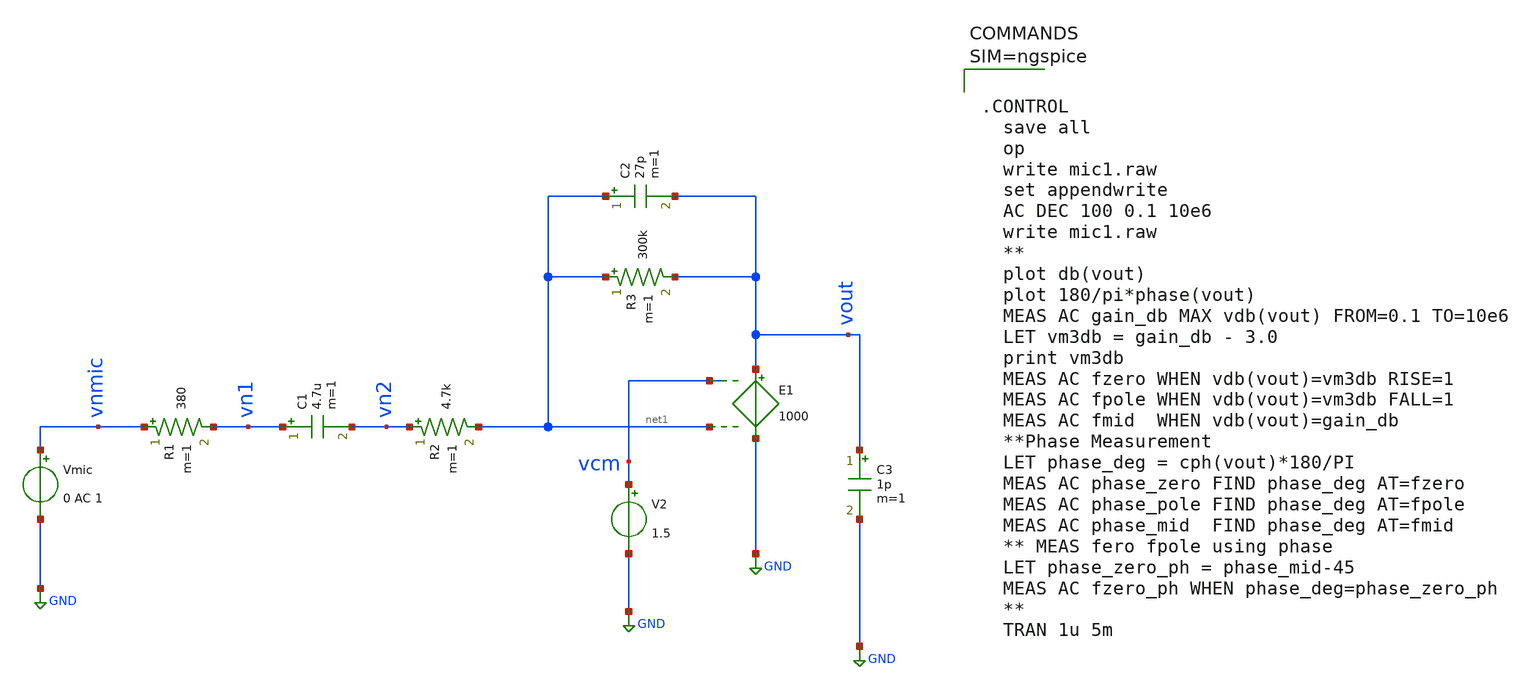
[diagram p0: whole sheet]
** sch_path: work/xschem/mic1.sch
**.subckt mic1
Vmic vnmic GND 0 AC 1
R1 vnmic vn1 380 m=1
R2 vn2 net1 4.7k m=1
C1 vn1 vn2 4.7u m=1
V2 vcm GND 1.5
C2 net1 vout 27p m=1
R3 net1 vout 300k m=1
C3 vout GND 1p m=1
E1 vout GND vcm net1 1000
**** begin user architecture code



.CONTROL
  save all
  op
  write mic1.raw
  set appendwrite
  AC DEC 100 0.1 10e6
  write mic1.raw
  **
  plot db(vout)
  plot 180/pi*phase(vout)
  MEAS AC gain_db MAX vdb(vout) FROM=0.1 TO=10e6
  LET vm3db = gain_db - 3.0
  print vm3db
  MEAS AC fzero WHEN vdb(vout)=vm3db RISE=1
  MEAS AC fpole WHEN vdb(vout)=vm3db FALL=1
  MEAS AC fmid  WHEN vdb(vout)=gain_db
  **Phase Measurement
  LET phase_deg = cph(vout)*180/PI
  MEAS AC phase_zero FIND phase_deg AT=fzero
  MEAS AC phase_pole FIND phase_deg AT=fpole
  MEAS AC phase_mid  FIND phase_deg AT=fmid
  ** MEAS fero fpole using phase
  LET phase_zero_ph = phase_mid-45
  MEAS AC fzero_ph WHEN phase_deg=phase_zero_ph
  **
  TRAN 1u 5m



**** end user architecture code
**.ends
.GLOBAL GND
.end
